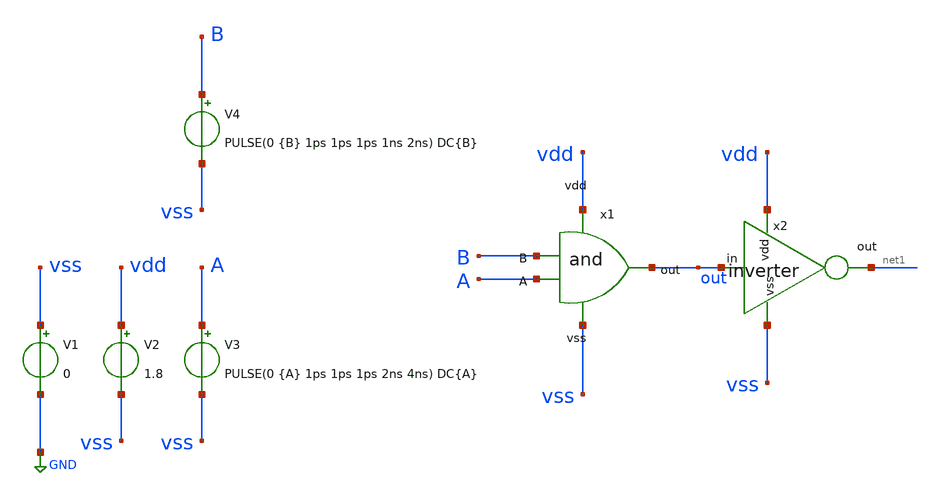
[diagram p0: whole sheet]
** sch_path: src/and/tb_and.sch
**.subckt tb_and
V1 vss GND 0
V2 vdd vss 1.8
V3 A vss PULSE(0 {A} 1ps 1ps 1ps 2ns 4ns) DC{A}
x2 vdd net1 out vss inverter
V4 B vss PULSE(0 {B} 1ps 1ps 1ps 1ns 2ns) DC{B}
x1 vdd B out A vss and
**** begin user architecture code


*Parametros
.param A=1.8
.param B=1.8
.param wni=0.45
.param wpi=0.9
.param wna=0.9
.param wpa=0.9

.options TEMP = 27.0

*Include
.lib /home/eamta/skywater/skywater-pdk/libraries/sky130_fd_pr_ngspice/latest/models/corners/sky130.lib TT

*Signal to Save
.save all   @M.x1.xM1.msky130_fd_pr__nfet_01v8[id]   @M.x1.xM2.msky130_fd_pr__nfet_01v8[id]   @M.x1.xM3.msky130_fd_pr__nfet_01v8[id]   @M.x1.xM4.msky130_fd_pr__pfet_01v8[id]  @M.x1.xM5.msky130_fd_pr__pfet_01v8[id]  @M.x1.xM6.msky130_fd_pr__pfet_01v8[id]   @M.x2.xM1.msky130_fd_pr__nfet_01v8[id]  @M.x2.xM2.msky130_fd_pr__pfet_01v8[id]

*Simulacion
.control

 dc v3 0 1.8 0.01 v4 1.8
 setplot dc
 plot v(out) v(A)
 *set filetype = ascii
 *write tb_and_dc.raw

 reset
 dc v4 0 1.8 0.01 v3 1.8
 setplot dc
 plot v(out) v(B)

 reset

 tran 0.01ns 10ns
 setplot transitorio
 plot v(out) v(A) v(B)
 set filetype= ascii
 write tb_and_tran.raw

.endc

.end


**** end user architecture code
**.ends

* expanding   symbol:  inverter/inverter.sym # of pins=4
** sym_path: src/inverter/inverter.sym
** sch_path: src/inverter/inverter.sch
.subckt inverter vdd out in vss
*.opin out
*.ipin in
*.ipin vss
*.ipin vdd
XM1 out in vss vss sky130_fd_pr__nfet_01v8 L=0.15 W=0.45 nf=1 ad='int((nf+1)/2) * W/nf * 0.29' as='int((nf+2)/2) * W/nf * 0.29'
+ pd='2*int((nf+1)/2) * (W/nf + 0.29)' ps='2*int((nf+2)/2) * (W/nf + 0.29)' nrd='0.29 / W' nrs='0.29 / W'
+ sa=0 sb=0 sd=0 mult=1 m=1
XM2 out in vdd vdd sky130_fd_pr__pfet_01v8 L=0.15 W=0.9 nf=1 ad='int((nf+1)/2) * W/nf * 0.29' as='int((nf+2)/2) * W/nf * 0.29'
+ pd='2*int((nf+1)/2) * (W/nf + 0.29)' ps='2*int((nf+2)/2) * (W/nf + 0.29)' nrd='0.29 / W' nrs='0.29 / W'
+ sa=0 sb=0 sd=0 mult=1 m=1
.ends


* expanding   symbol:  and/and.sym # of pins=5
** sym_path: src/and/and.sym
** sch_path: src/and/and.sch
.subckt and vdd B out A vss
*.ipin vdd
*.ipin vss
*.opin out
*.ipin B
*.ipin A
XM1 net2 A vss vss sky130_fd_pr__nfet_01v8 L=0.15 W={wna} nf=1 ad='int((nf+1)/2) * W/nf * 0.29' as='int((nf+2)/2) * W/nf * 0.29'
+ pd='2*int((nf+1)/2) * (W/nf + 0.29)' ps='2*int((nf+2)/2) * (W/nf + 0.29)' nrd='0.29 / W' nrs='0.29 / W'
+ sa=0 sb=0 sd=0 mult=1 m=1
XM2 net1 B vdd vdd sky130_fd_pr__pfet_01v8 L=0.15 W={wpa} nf=1 ad='int((nf+1)/2) * W/nf * 0.29' as='int((nf+2)/2) * W/nf * 0.29'
+ pd='2*int((nf+1)/2) * (W/nf + 0.29)' ps='2*int((nf+2)/2) * (W/nf + 0.29)' nrd='0.29 / W' nrs='0.29 / W'
+ sa=0 sb=0 sd=0 mult=1 m=1
XM3 net1 B net2 vss sky130_fd_pr__nfet_01v8 L=0.15 W={wna} nf=1 ad='int((nf+1)/2) * W/nf * 0.29' as='int((nf+2)/2) * W/nf * 0.29'
+ pd='2*int((nf+1)/2) * (W/nf + 0.29)' ps='2*int((nf+2)/2) * (W/nf + 0.29)' nrd='0.29 / W' nrs='0.29 / W'
+ sa=0 sb=0 sd=0 mult=1 m=1
XM4 net1 A vdd vdd sky130_fd_pr__pfet_01v8 L=0.15 W={wpa} nf=1 ad='int((nf+1)/2) * W/nf * 0.29' as='int((nf+2)/2) * W/nf * 0.29'
+ pd='2*int((nf+1)/2) * (W/nf + 0.29)' ps='2*int((nf+2)/2) * (W/nf + 0.29)' nrd='0.29 / W' nrs='0.29 / W'
+ sa=0 sb=0 sd=0 mult=1 m=1
XM5 out net1 vss vss sky130_fd_pr__nfet_01v8 L=0.15 W={wni} nf=1 ad='int((nf+1)/2) * W/nf * 0.29' as='int((nf+2)/2) * W/nf * 0.29'
+ pd='2*int((nf+1)/2) * (W/nf + 0.29)' ps='2*int((nf+2)/2) * (W/nf + 0.29)' nrd='0.29 / W' nrs='0.29 / W'
+ sa=0 sb=0 sd=0 mult=1 m=1
XM6 out net1 vdd vdd sky130_fd_pr__pfet_01v8 L=0.15 W={wpi} nf=1 ad='int((nf+1)/2) * W/nf * 0.29' as='int((nf+2)/2) * W/nf * 0.29'
+ pd='2*int((nf+1)/2) * (W/nf + 0.29)' ps='2*int((nf+2)/2) * (W/nf + 0.29)' nrd='0.29 / W' nrs='0.29 / W'
+ sa=0 sb=0 sd=0 mult=1 m=1
.ends

.GLOBAL GND
.end
